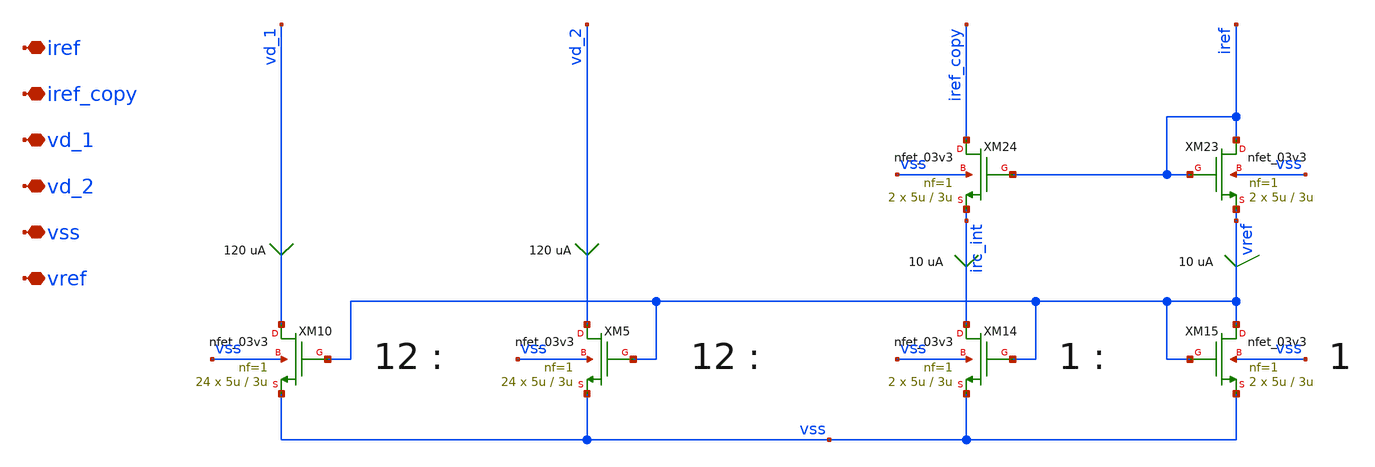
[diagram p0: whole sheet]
** sch_path: xschem/ota/s1_nmos_bias.sch
**.subckt s1_nmos_bias iref iref_copy vd_1 vd_2 vss vref
*.iopin iref
*.iopin iref_copy
*.iopin vd_1
*.iopin vd_2
*.iopin vss
*.iopin vref
XM14 irc_int vref vss vss nfet_03v3 L=3u W=5u nf=1 ad='int((nf+1)/2) * W/nf * 0.18u' as='int((nf+2)/2) * W/nf * 0.18u'
+ pd='2*int((nf+1)/2) * (W/nf + 0.18u)' ps='2*int((nf+2)/2) * (W/nf + 0.18u)' nrd='0.18u / W' nrs='0.18u / W'
+ sa=0 sb=0 sd=0 m=2
XM15 vref vref vss vss nfet_03v3 L=3u W=5u nf=1 ad='int((nf+1)/2) * W/nf * 0.18u' as='int((nf+2)/2) * W/nf * 0.18u'
+ pd='2*int((nf+1)/2) * (W/nf + 0.18u)' ps='2*int((nf+2)/2) * (W/nf + 0.18u)' nrd='0.18u / W' nrs='0.18u / W'
+ sa=0 sb=0 sd=0 m=2
XM10 vd_1 vref vss vss nfet_03v3 L=3u W=5u nf=1 ad='int((nf+1)/2) * W/nf * 0.18u' as='int((nf+2)/2) * W/nf * 0.18u'
+ pd='2*int((nf+1)/2) * (W/nf + 0.18u)' ps='2*int((nf+2)/2) * (W/nf + 0.18u)' nrd='0.18u / W' nrs='0.18u / W'
+ sa=0 sb=0 sd=0 m=24
XM5 vd_2 vref vss vss nfet_03v3 L=3u W=5u nf=1 ad='int((nf+1)/2) * W/nf * 0.18u' as='int((nf+2)/2) * W/nf * 0.18u'
+ pd='2*int((nf+1)/2) * (W/nf + 0.18u)' ps='2*int((nf+2)/2) * (W/nf + 0.18u)' nrd='0.18u / W' nrs='0.18u / W'
+ sa=0 sb=0 sd=0 m=24
XM23 iref iref vref vss nfet_03v3 L=3u W=5u nf=1 ad='int((nf+1)/2) * W/nf * 0.18u' as='int((nf+2)/2) * W/nf * 0.18u'
+ pd='2*int((nf+1)/2) * (W/nf + 0.18u)' ps='2*int((nf+2)/2) * (W/nf + 0.18u)' nrd='0.18u / W' nrs='0.18u / W'
+ sa=0 sb=0 sd=0 m=2
XM24 iref_copy iref irc_int vss nfet_03v3 L=3u W=5u nf=1 ad='int((nf+1)/2) * W/nf * 0.18u' as='int((nf+2)/2) * W/nf * 0.18u'
+ pd='2*int((nf+1)/2) * (W/nf + 0.18u)' ps='2*int((nf+2)/2) * (W/nf + 0.18u)' nrd='0.18u / W' nrs='0.18u / W'
+ sa=0 sb=0 sd=0 m=2
**.ends
.end
